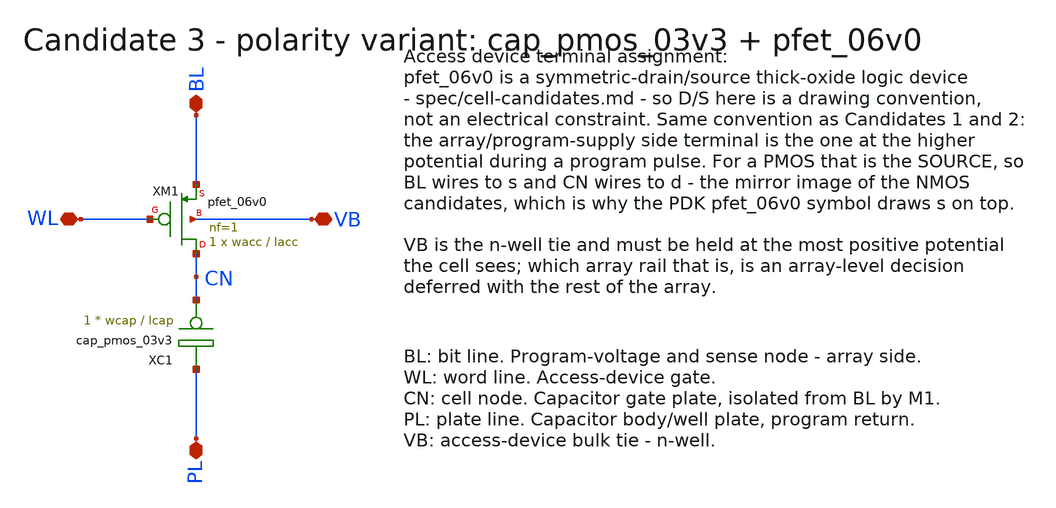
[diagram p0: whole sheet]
** sch_path: design/cells/cell_candidate3.sch
**.subckt cell_candidate3 BL WL PL VB
*.iopin BL
*.iopin WL
*.iopin PL
*.iopin VB
XM1 CN WL BL VB pfet_06v0 L=lacc W=wacc nf=1 ad='int((nf+1)/2) * wacc/nf * 0.18u' as='int((nf+2)/2) * wacc/nf * 0.18u'
+ pd='2*int((nf+1)/2) * (wacc/nf + 0.18u)' ps='2*int((nf+2)/2) * (wacc/nf + 0.18u)' nrd='0.18u / wacc'
+ nrs='0.18u / wacc' sa=0 sb=0 sd=0 m=1
XC1 CN PL cap_pmos_03v3 c_width=wcap c_length=lcap m=1
**.ends
.end
